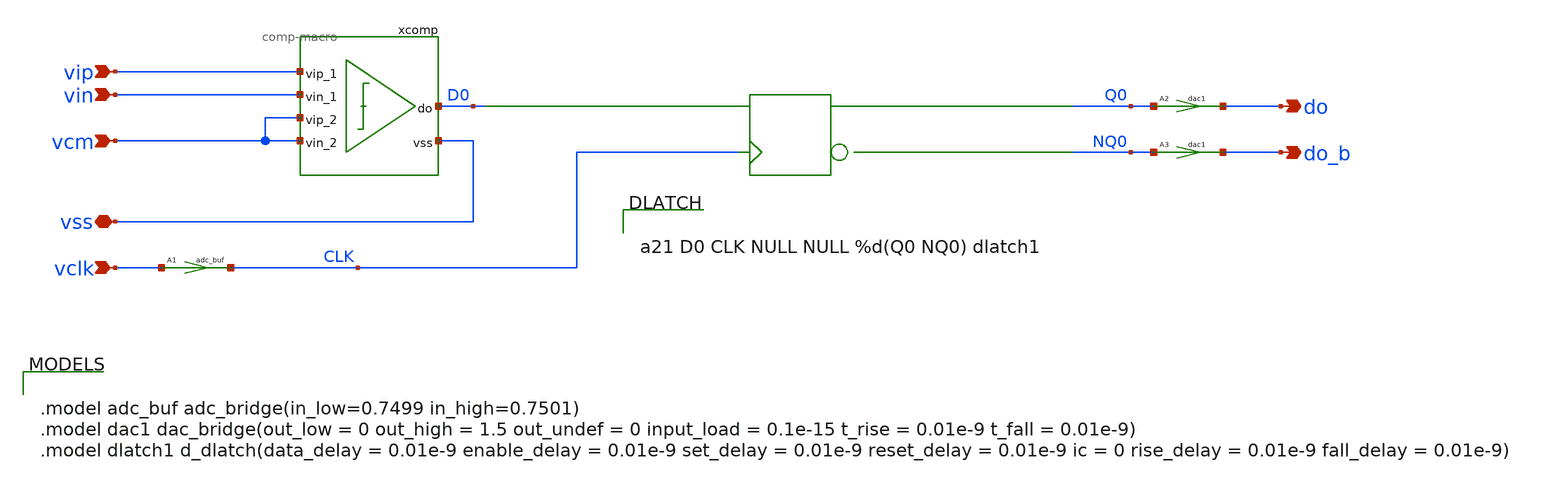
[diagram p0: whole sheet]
** sch_path: xschem/adc-1b-ideal.sch
**.subckt adc-1b-ideal vss vip vin vcm vclk do_b do
*.iopin vss
*.ipin vip
*.ipin vin
*.ipin vcm
*.ipin vclk
*.opin do_b
*.opin do
A1 [ vclk ] [ CLK ] adc_buf
A3 [ NQ0 ] [ do_b ] dac1
A2 [ Q0 ] [ do ] dac1
xcomp D0 vip vin vcm vcm vss comp-macro
**.ends

* expanding   symbol:  comp-macro.sym # of pins=6
** sym_path: xschem/comp-macro.sym
** sch_path: xschem/comp-macro.sch
.subckt comp-macro do vip_1 vin_1 vip_2 vin_2 vss
*.iopin vss
*.ipin vip_1
*.ipin vin_1
*.ipin vip_2
*.ipin vin_2
*.opin do
A1 [ net1 ] [ do ] comp0
E1 net1 net2 vip_1 vin_1 1
E2 net2 vss vip_2 vin_2 1
**** begin user architecture code

.model comp0 adc_bridge(in_low=-0.0001 in_high=0.0001)

**** end user architecture code
.ends

**** begin user architecture code


.model adc_buf adc_bridge(in_low=0.7499 in_high=0.7501)
.model dac1 dac_bridge(out_low = 0 out_high = 1.5 out_undef = 0 input_load = 0.1e-15 t_rise =
+ 0.01e-9 t_fall = 0.01e-9)
.model dlatch1 d_dlatch(data_delay = 0.01e-9 enable_delay = 0.01e-9 set_delay = 0.01e-9 reset_delay
+ = 0.01e-9 ic = 0 rise_delay = 0.01e-9 fall_delay = 0.01e-9)



a21 D0 CLK NULL NULL %d(Q0 NQ0) dlatch1


**** end user architecture code
.end
